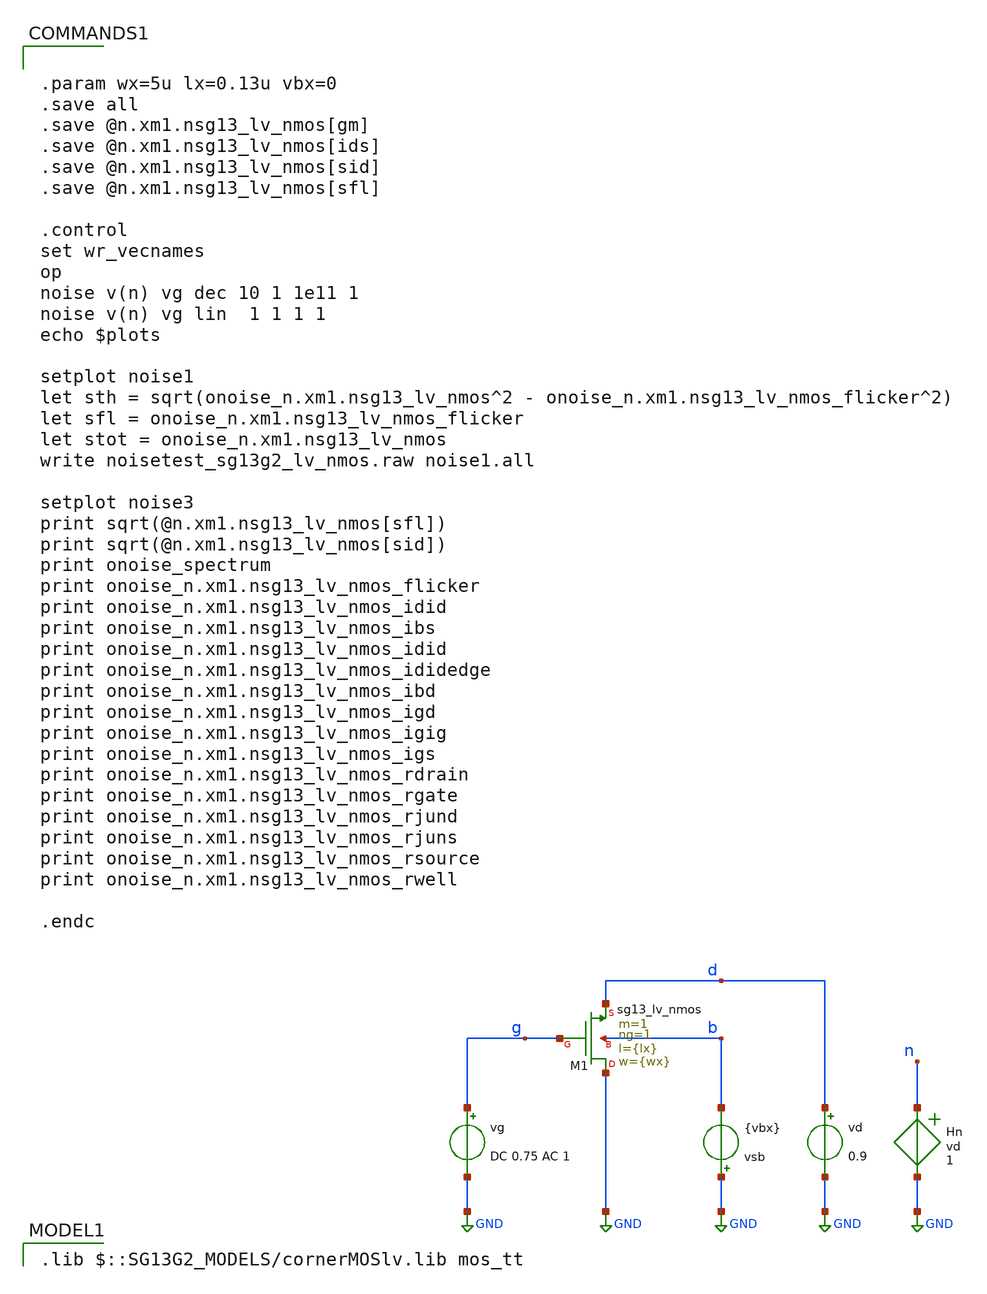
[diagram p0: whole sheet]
** sch_path: xschem/noisetest_sg13g2_lv_nmos.sch
**.subckt noisetest_sg13g2_lv_nmos
vg g GND DC 0.75 AC 1
vd d GND 0.9
vsb GND b {vbx}
Hn n GND vd 1
XM1 GND g d b sg13_lv_nmos w={wx} l={lx} ng=1 m=1 mm_ok=1
**** begin user architecture code


.param wx=5u lx=0.13u vbx=0
.save all
.save @n.xm1.nsg13_lv_nmos[gm]
.save @n.xm1.nsg13_lv_nmos[ids]
.save @n.xm1.nsg13_lv_nmos[sid]
.save @n.xm1.nsg13_lv_nmos[sfl]

.control
set wr_vecnames
op
noise v(n) vg dec 10 1 1e11 1
noise v(n) vg lin  1 1 1 1
echo $plots

setplot noise1
let sth = sqrt(onoise_n.xm1.nsg13_lv_nmos^2 - onoise_n.xm1.nsg13_lv_nmos_flicker^2)
let sfl = onoise_n.xm1.nsg13_lv_nmos_flicker
let stot = onoise_n.xm1.nsg13_lv_nmos
write noisetest_sg13g2_lv_nmos.raw noise1.all

setplot noise3
print sqrt(@n.xm1.nsg13_lv_nmos[sfl])
print sqrt(@n.xm1.nsg13_lv_nmos[sid])
print onoise_spectrum
print onoise_n.xm1.nsg13_lv_nmos_flicker
print onoise_n.xm1.nsg13_lv_nmos_idid
print onoise_n.xm1.nsg13_lv_nmos_ibs
print onoise_n.xm1.nsg13_lv_nmos_idid
print onoise_n.xm1.nsg13_lv_nmos_ididedge
print onoise_n.xm1.nsg13_lv_nmos_ibd
print onoise_n.xm1.nsg13_lv_nmos_igd
print onoise_n.xm1.nsg13_lv_nmos_igig
print onoise_n.xm1.nsg13_lv_nmos_igs
print onoise_n.xm1.nsg13_lv_nmos_rdrain
print onoise_n.xm1.nsg13_lv_nmos_rgate
print onoise_n.xm1.nsg13_lv_nmos_rjund
print onoise_n.xm1.nsg13_lv_nmos_rjuns
print onoise_n.xm1.nsg13_lv_nmos_rsource
print onoise_n.xm1.nsg13_lv_nmos_rwell

.endc


 .lib $::SG13G2_MODELS/cornerMOSlv.lib mos_tt

**** end user architecture code
**.ends
.GLOBAL GND
.end
